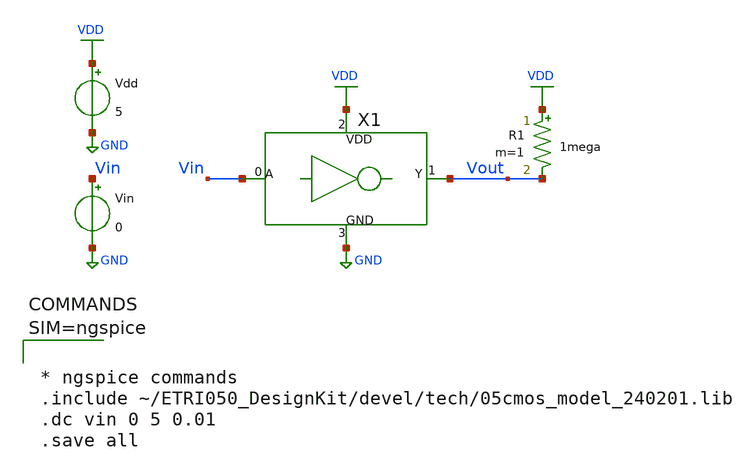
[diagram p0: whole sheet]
** sch_path: Tutorials/1-1_Inverter_XSchem/inverter_TB.sch
**.subckt inverter_TB
X1 Vin Vout VDD GND inverter
Vdd VDD GND 5
Vin Vin GND 0
R1 VDD Vout 1mega m=1
**** begin user architecture code



* ngspice commands
.include ~/ETRI050_DesignKit/devel/tech/05cmos_model_240201.lib
.dc vin 0 5 0.01
.save all



**** end user architecture code
**.ends
.GLOBAL VDD
.GLOBAL GND
.end
